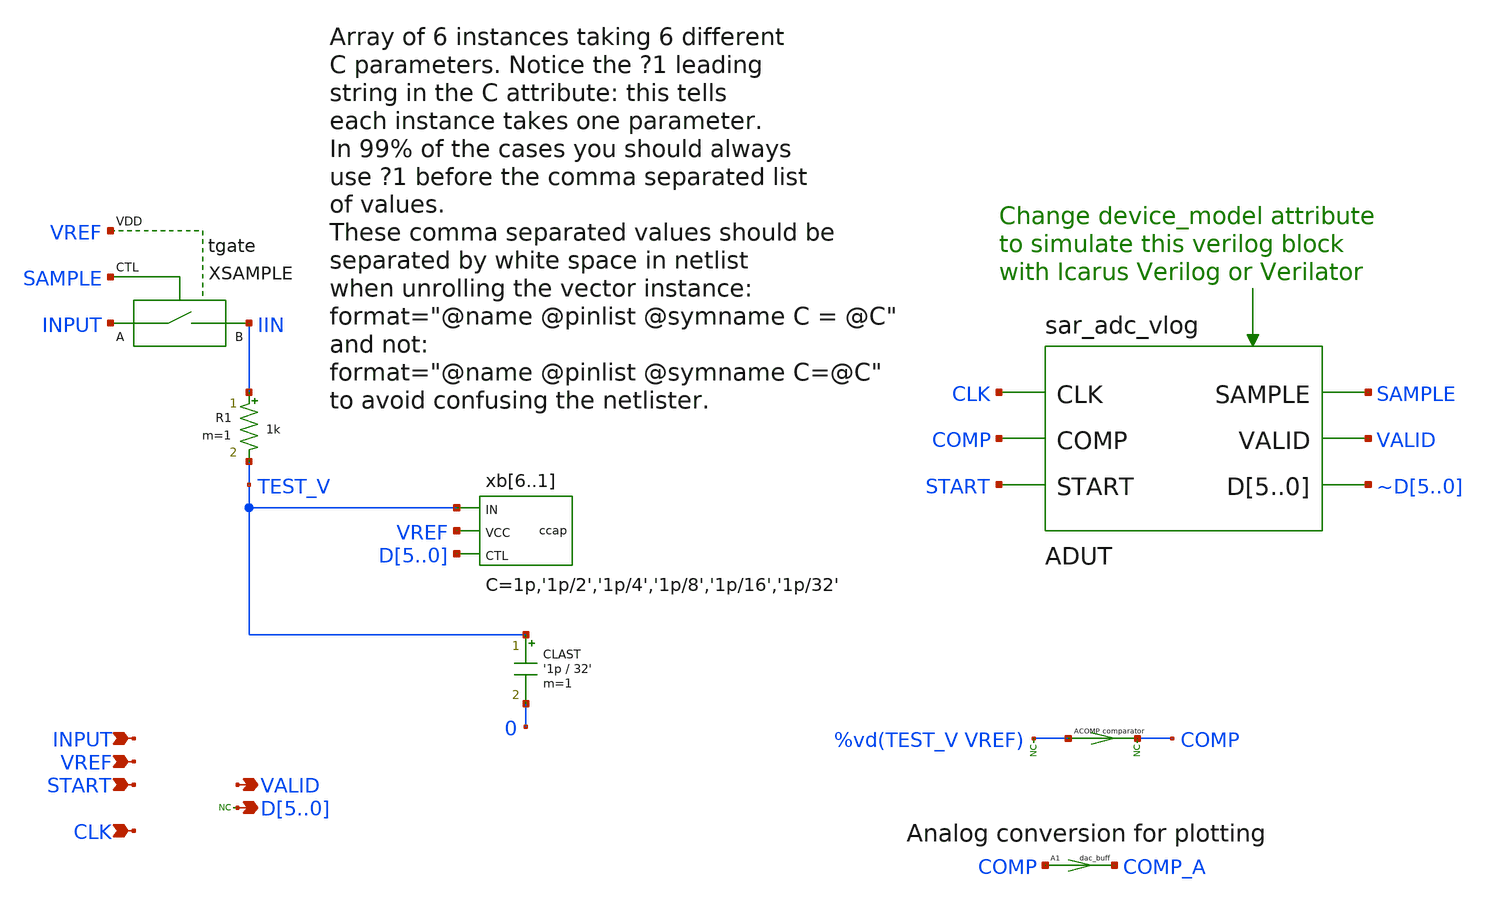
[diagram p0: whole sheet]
** sch_path: xschem_library/ngspice_verilog_cosim/sar_adc.sch
**.subckt sar_adc INPUT VREF START VALID CLK D5,D4,D3,D2,D1,D0
*.ipin INPUT
*.ipin VREF
*.ipin START
*.opin VALID
*.ipin CLK
*.opin D5,D4,D3,D2,D1,D0
CLAST TEST_V 0 '1p / 32' m=1
ACOMP [ %vd(TEST_V VREF) ] [ COMP ] comparator
XSAMPLE INPUT IIN SAMPLE VREF tgate
R1 IIN TEST_V 1k m=1
ADUT [ CLK COMP START ] [ SAMPLE VALID ~D5 ~D4 ~D3 ~D2 ~D1 ~D0 ] dut
A1 [ COMP ] [ COMP_A ] dac_buff
* noconn D[5..0]
* noconn COMP
* noconn %vd(TEST_V VREF)
xb6 TEST_V VREF D5 ccap C = 1p
xb5 TEST_V VREF D4 ccap C = '1p/2'
xb4 TEST_V VREF D3 ccap C = '1p/4'
xb3 TEST_V VREF D2 ccap C = '1p/8'
xb2 TEST_V VREF D1 ccap C = '1p/16'
xb1 TEST_V VREF D0 ccap C = '1p/32'
**.ends

* expanding   symbol:  tgate.sym # of pins=4
** sym_path: xschem_library/ngspice_verilog_cosim/tgate.sym
** sch_path: xschem_library/ngspice_verilog_cosim/tgate.sch
.subckt tgate A B CTL VDD
*.ipin CTL
*.iopin B
*.iopin A
*.ipin VDD
SWITCH A B CTL 0 TG
* noconn VDD
.ends


* expanding   symbol:  ccap.sym # of pins=3
** sym_path: xschem_library/ngspice_verilog_cosim/ccap.sym
** sch_path: xschem_library/ngspice_verilog_cosim/ccap.sch
.subckt ccap IN VCC CTL  C=1p
*.ipin IN
*.ipin VCC
*.ipin CTL
XINV CTL TAIL VCC ainv
CB IN TAIL c='C' m=1
.ends


* expanding   symbol:  ainv.sym # of pins=3
** sym_path: xschem_library/ngspice_verilog_cosim/ainv.sym
** sch_path: xschem_library/ngspice_verilog_cosim/ainv.sch
.subckt ainv IN OUT VDD
*.ipin IN
*.opin OUT
*.ipin VDD
MN OUT IN 0 0 N1
MP OUT IN VDD VDD P1
.ends

**** begin user architecture code
.model dut d_cosim simulation="ivlng" sim_args=["adc"]
.model comparator adc_bridge in_low=0 in_high=0
.model n1 nmos   level=2 vto=0.5 kp=24e-6 gamma=0.15 phi=0.65 lambda=0.015 xj=0.5e-6

.model p1 pmos   level=2 vto=-0.5 kp=8.5e-6 gamma=0.4 phi=0.65 lambda=0.05 xj=0.5e-6

.MODEL TG SW( VT=1.5 RON=2k )
.model dac_buff dac_bridge input_load=1e-15 t_rise=10n t_fall=10n  out_low=0 out_high=3.3
**** end user architecture code
.end
